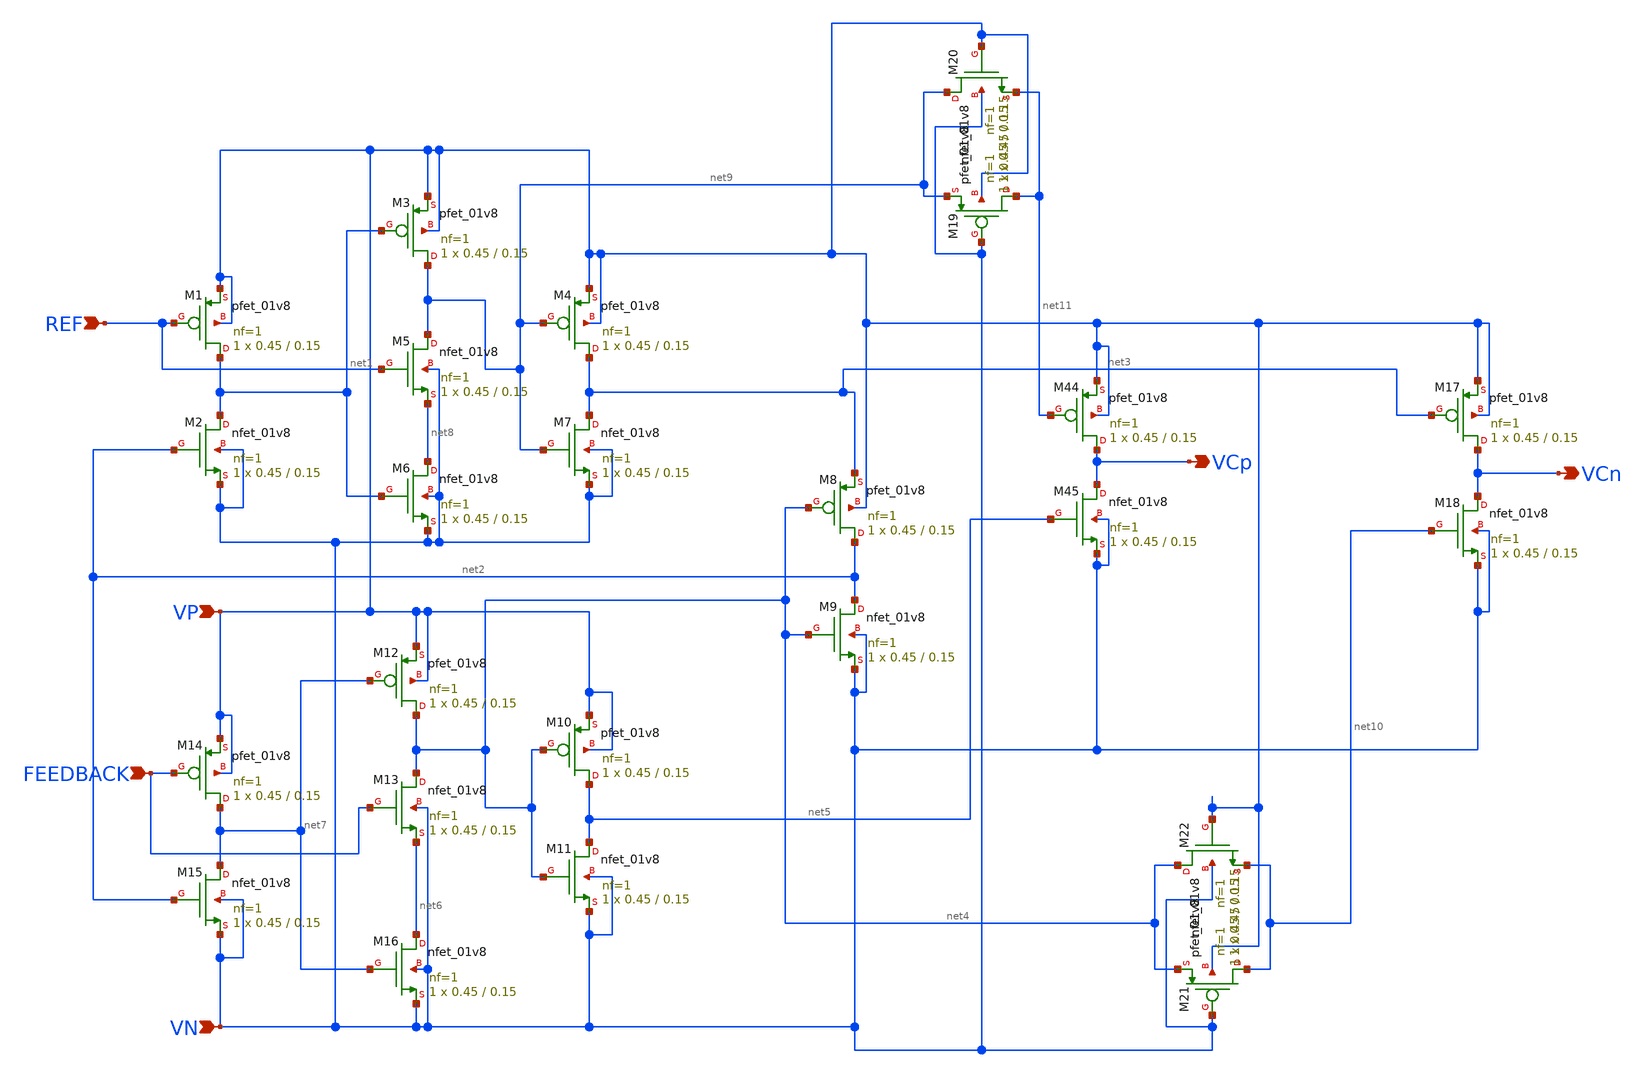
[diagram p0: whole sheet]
** sch_path: xschem_sch/pfd_ver6.sch
**.subckt pfd_ver6 VCn REF FEEDBACK VCp VP VN
*.opin VCn
*.ipin REF
*.ipin FEEDBACK
*.opin VCp
*.ipin VP
*.ipin VN
XM1 net1 REF VP VP sky130_fd_pr__pfet_01v8 L=0.15 W=0.45 nf=1 ad='int((nf+1)/2) * W/nf * 0.29' as='int((nf+2)/2) * W/nf * 0.29'
+ pd='2*int((nf+1)/2) * (W/nf + 0.29)' ps='2*int((nf+2)/2) * (W/nf + 0.29)' nrd='0.29 / W' nrs='0.29 / W'
+ sa=0 sb=0 sd=0 mult=1 m=1
XM2 net1 net2 VN VN sky130_fd_pr__nfet_01v8 L=0.15 W=0.45 nf=1 ad='int((nf+1)/2) * W/nf * 0.29' as='int((nf+2)/2) * W/nf * 0.29'
+ pd='2*int((nf+1)/2) * (W/nf + 0.29)' ps='2*int((nf+2)/2) * (W/nf + 0.29)' nrd='0.29 / W' nrs='0.29 / W'
+ sa=0 sb=0 sd=0 mult=1 m=1
XM3 net9 net1 VP VP sky130_fd_pr__pfet_01v8 L=0.15 W=0.45 nf=1 ad='int((nf+1)/2) * W/nf * 0.29' as='int((nf+2)/2) * W/nf * 0.29'
+ pd='2*int((nf+1)/2) * (W/nf + 0.29)' ps='2*int((nf+2)/2) * (W/nf + 0.29)' nrd='0.29 / W' nrs='0.29 / W'
+ sa=0 sb=0 sd=0 mult=1 m=1
XM4 net3 net9 VP VP sky130_fd_pr__pfet_01v8 L=0.15 W=0.45 nf=1 ad='int((nf+1)/2) * W/nf * 0.29' as='int((nf+2)/2) * W/nf * 0.29'
+ pd='2*int((nf+1)/2) * (W/nf + 0.29)' ps='2*int((nf+2)/2) * (W/nf + 0.29)' nrd='0.29 / W' nrs='0.29 / W'
+ sa=0 sb=0 sd=0 mult=1 m=1
XM5 net9 REF net8 VN sky130_fd_pr__nfet_01v8 L=0.15 W=0.45 nf=1 ad='int((nf+1)/2) * W/nf * 0.29' as='int((nf+2)/2) * W/nf * 0.29'
+ pd='2*int((nf+1)/2) * (W/nf + 0.29)' ps='2*int((nf+2)/2) * (W/nf + 0.29)' nrd='0.29 / W' nrs='0.29 / W'
+ sa=0 sb=0 sd=0 mult=1 m=1
XM6 net8 net1 VN VN sky130_fd_pr__nfet_01v8 L=0.15 W=0.45 nf=1 ad='int((nf+1)/2) * W/nf * 0.29' as='int((nf+2)/2) * W/nf * 0.29'
+ pd='2*int((nf+1)/2) * (W/nf + 0.29)' ps='2*int((nf+2)/2) * (W/nf + 0.29)' nrd='0.29 / W' nrs='0.29 / W'
+ sa=0 sb=0 sd=0 mult=1 m=1
XM7 net3 net9 VN VN sky130_fd_pr__nfet_01v8 L=0.15 W=0.45 nf=1 ad='int((nf+1)/2) * W/nf * 0.29' as='int((nf+2)/2) * W/nf * 0.29'
+ pd='2*int((nf+1)/2) * (W/nf + 0.29)' ps='2*int((nf+2)/2) * (W/nf + 0.29)' nrd='0.29 / W' nrs='0.29 / W'
+ sa=0 sb=0 sd=0 mult=1 m=1
XM8 net2 net4 net3 VP sky130_fd_pr__pfet_01v8 L=0.15 W=0.45 nf=1 ad='int((nf+1)/2) * W/nf * 0.29' as='int((nf+2)/2) * W/nf * 0.29'
+ pd='2*int((nf+1)/2) * (W/nf + 0.29)' ps='2*int((nf+2)/2) * (W/nf + 0.29)' nrd='0.29 / W' nrs='0.29 / W'
+ sa=0 sb=0 sd=0 mult=1 m=1
XM9 net2 net4 VN VN sky130_fd_pr__nfet_01v8 L=0.15 W=0.45 nf=1 ad='int((nf+1)/2) * W/nf * 0.29' as='int((nf+2)/2) * W/nf * 0.29'
+ pd='2*int((nf+1)/2) * (W/nf + 0.29)' ps='2*int((nf+2)/2) * (W/nf + 0.29)' nrd='0.29 / W' nrs='0.29 / W'
+ sa=0 sb=0 sd=0 mult=1 m=1
XM10 net5 net4 VP VP sky130_fd_pr__pfet_01v8 L=0.15 W=0.45 nf=1 ad='int((nf+1)/2) * W/nf * 0.29' as='int((nf+2)/2) * W/nf * 0.29'
+ pd='2*int((nf+1)/2) * (W/nf + 0.29)' ps='2*int((nf+2)/2) * (W/nf + 0.29)' nrd='0.29 / W' nrs='0.29 / W'
+ sa=0 sb=0 sd=0 mult=1 m=1
XM11 net5 net4 VN VN sky130_fd_pr__nfet_01v8 L=0.15 W=0.45 nf=1 ad='int((nf+1)/2) * W/nf * 0.29' as='int((nf+2)/2) * W/nf * 0.29'
+ pd='2*int((nf+1)/2) * (W/nf + 0.29)' ps='2*int((nf+2)/2) * (W/nf + 0.29)' nrd='0.29 / W' nrs='0.29 / W'
+ sa=0 sb=0 sd=0 mult=1 m=1
XM12 net4 net7 VP VP sky130_fd_pr__pfet_01v8 L=0.15 W=0.45 nf=1 ad='int((nf+1)/2) * W/nf * 0.29' as='int((nf+2)/2) * W/nf * 0.29'
+ pd='2*int((nf+1)/2) * (W/nf + 0.29)' ps='2*int((nf+2)/2) * (W/nf + 0.29)' nrd='0.29 / W' nrs='0.29 / W'
+ sa=0 sb=0 sd=0 mult=1 m=1
XM13 net4 FEEDBACK net6 VN sky130_fd_pr__nfet_01v8 L=0.15 W=0.45 nf=1 ad='int((nf+1)/2) * W/nf * 0.29'
+ as='int((nf+2)/2) * W/nf * 0.29' pd='2*int((nf+1)/2) * (W/nf + 0.29)' ps='2*int((nf+2)/2) * (W/nf + 0.29)'
+ nrd='0.29 / W' nrs='0.29 / W' sa=0 sb=0 sd=0 mult=1 m=1
XM14 net7 FEEDBACK VP VP sky130_fd_pr__pfet_01v8 L=0.15 W=0.45 nf=1 ad='int((nf+1)/2) * W/nf * 0.29'
+ as='int((nf+2)/2) * W/nf * 0.29' pd='2*int((nf+1)/2) * (W/nf + 0.29)' ps='2*int((nf+2)/2) * (W/nf + 0.29)'
+ nrd='0.29 / W' nrs='0.29 / W' sa=0 sb=0 sd=0 mult=1 m=1
XM15 net7 net2 VN VN sky130_fd_pr__nfet_01v8 L=0.15 W=0.45 nf=1 ad='int((nf+1)/2) * W/nf * 0.29' as='int((nf+2)/2) * W/nf * 0.29'
+ pd='2*int((nf+1)/2) * (W/nf + 0.29)' ps='2*int((nf+2)/2) * (W/nf + 0.29)' nrd='0.29 / W' nrs='0.29 / W'
+ sa=0 sb=0 sd=0 mult=1 m=1
XM16 net6 net7 VN VN sky130_fd_pr__nfet_01v8 L=0.15 W=0.45 nf=1 ad='int((nf+1)/2) * W/nf * 0.29' as='int((nf+2)/2) * W/nf * 0.29'
+ pd='2*int((nf+1)/2) * (W/nf + 0.29)' ps='2*int((nf+2)/2) * (W/nf + 0.29)' nrd='0.29 / W' nrs='0.29 / W'
+ sa=0 sb=0 sd=0 mult=1 m=1
XM45 VCp net5 VN VN sky130_fd_pr__nfet_01v8 L=0.15 W=0.45 nf=1 ad='int((nf+1)/2) * W/nf * 0.29' as='int((nf+2)/2) * W/nf * 0.29'
+ pd='2*int((nf+1)/2) * (W/nf + 0.29)' ps='2*int((nf+2)/2) * (W/nf + 0.29)' nrd='0.29 / W' nrs='0.29 / W'
+ sa=0 sb=0 sd=0 mult=1 m=1
XM44 VCp net11 VP VP sky130_fd_pr__pfet_01v8 L=0.15 W=0.45 nf=1 ad='int((nf+1)/2) * W/nf * 0.29' as='int((nf+2)/2) * W/nf * 0.29'
+ pd='2*int((nf+1)/2) * (W/nf + 0.29)' ps='2*int((nf+2)/2) * (W/nf + 0.29)' nrd='0.29 / W' nrs='0.29 / W'
+ sa=0 sb=0 sd=0 mult=1 m=1
XM17 VCn net3 VP VP sky130_fd_pr__pfet_01v8 L=0.15 W=0.45 nf=1 ad='int((nf+1)/2) * W/nf * 0.29' as='int((nf+2)/2) * W/nf * 0.29'
+ pd='2*int((nf+1)/2) * (W/nf + 0.29)' ps='2*int((nf+2)/2) * (W/nf + 0.29)' nrd='0.29 / W' nrs='0.29 / W'
+ sa=0 sb=0 sd=0 mult=1 m=1
XM18 VCn net10 VN VN sky130_fd_pr__nfet_01v8 L=0.15 W=0.45 nf=1 ad='int((nf+1)/2) * W/nf * 0.29' as='int((nf+2)/2) * W/nf * 0.29'
+ pd='2*int((nf+1)/2) * (W/nf + 0.29)' ps='2*int((nf+2)/2) * (W/nf + 0.29)' nrd='0.29 / W' nrs='0.29 / W'
+ sa=0 sb=0 sd=0 mult=1 m=1
XM19 net11 VN net9 VP sky130_fd_pr__pfet_01v8 L=0.15 W=0.45 nf=1 ad='int((nf+1)/2) * W/nf * 0.29' as='int((nf+2)/2) * W/nf * 0.29'
+ pd='2*int((nf+1)/2) * (W/nf + 0.29)' ps='2*int((nf+2)/2) * (W/nf + 0.29)' nrd='0.29 / W' nrs='0.29 / W'
+ sa=0 sb=0 sd=0 mult=1 m=1
XM20 net9 VP net11 VN sky130_fd_pr__nfet_01v8 L=0.15 W=0.45 nf=1 ad='int((nf+1)/2) * W/nf * 0.29' as='int((nf+2)/2) * W/nf * 0.29'
+ pd='2*int((nf+1)/2) * (W/nf + 0.29)' ps='2*int((nf+2)/2) * (W/nf + 0.29)' nrd='0.29 / W' nrs='0.29 / W'
+ sa=0 sb=0 sd=0 mult=1 m=1
XM21 net10 VN net4 VP sky130_fd_pr__pfet_01v8 L=0.15 W=0.45 nf=1 ad='int((nf+1)/2) * W/nf * 0.29' as='int((nf+2)/2) * W/nf * 0.29'
+ pd='2*int((nf+1)/2) * (W/nf + 0.29)' ps='2*int((nf+2)/2) * (W/nf + 0.29)' nrd='0.29 / W' nrs='0.29 / W'
+ sa=0 sb=0 sd=0 mult=1 m=1
XM22 net4 VP net10 VN sky130_fd_pr__nfet_01v8 L=0.15 W=0.45 nf=1 ad='int((nf+1)/2) * W/nf * 0.29' as='int((nf+2)/2) * W/nf * 0.29'
+ pd='2*int((nf+1)/2) * (W/nf + 0.29)' ps='2*int((nf+2)/2) * (W/nf + 0.29)' nrd='0.29 / W' nrs='0.29 / W'
+ sa=0 sb=0 sd=0 mult=1 m=1
**.ends
.end
